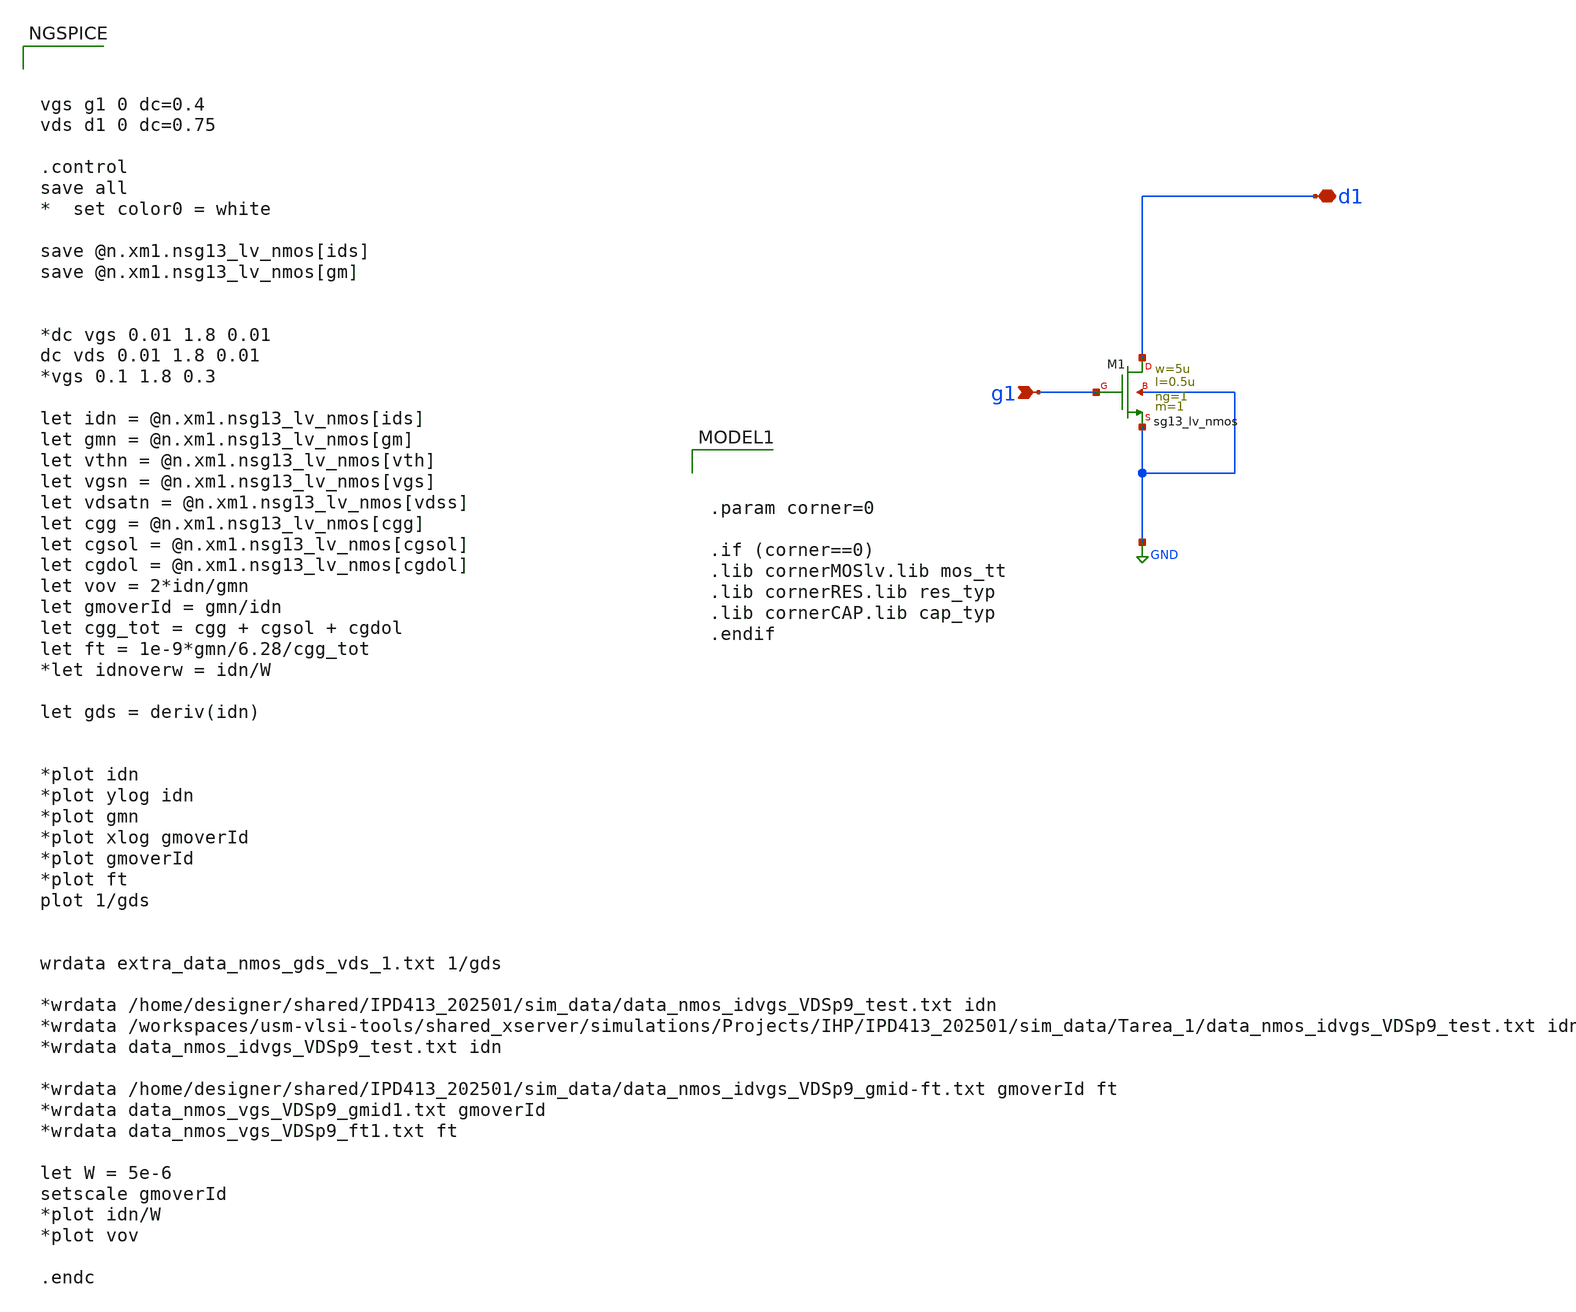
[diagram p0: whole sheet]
** sch_path: others/single mos/tb_nmoslv_charac.sch
**.subckt tb_nmoslv_charac g1 d1
*.ipin g1
*.iopin d1
XM1 d1 g1 GND GND sg13_lv_nmos w=5u l=0.5u ng=1 m=1 mm_ok=1
**** begin user architecture code



vgs g1 0 dc=0.4
vds d1 0 dc=0.75

.control
save all
*  set color0 = white

save @n.xm1.nsg13_lv_nmos[ids]
save @n.xm1.nsg13_lv_nmos[gm]


*dc vgs 0.01 1.8 0.01
dc vds 0.01 1.8 0.01
*vgs 0.1 1.8 0.3

let idn = @n.xm1.nsg13_lv_nmos[ids]
let gmn = @n.xm1.nsg13_lv_nmos[gm]
let vthn = @n.xm1.nsg13_lv_nmos[vth]
let vgsn = @n.xm1.nsg13_lv_nmos[vgs]
let vdsatn = @n.xm1.nsg13_lv_nmos[vdss]
let cgg = @n.xm1.nsg13_lv_nmos[cgg]
let cgsol = @n.xm1.nsg13_lv_nmos[cgsol]
let cgdol = @n.xm1.nsg13_lv_nmos[cgdol]
let vov = 2*idn/gmn
let gmoverId = gmn/idn
let cgg_tot = cgg + cgsol + cgdol
let ft = 1e-9*gmn/6.28/cgg_tot
*let idnoverw = idn/W

let gds = deriv(idn)


*plot idn
*plot ylog idn
*plot gmn
*plot xlog gmoverId
*plot gmoverId
*plot ft
plot 1/gds


wrdata extra_data_nmos_gds_vds_1.txt 1/gds

*wrdata /home/designer/shared/IPD413_202501/sim_data/data_nmos_idvgs_VDSp9_test.txt idn
*wrdata
*+ /workspaces/usm-vlsi-tools/shared_xserver/simulations/Projects/IHP/IPD413_202501/sim_data/Tarea_1/data_nmos_idvgs_VDSp9_test.txt idn
*wrdata data_nmos_idvgs_VDSp9_test.txt idn

*wrdata /home/designer/shared/IPD413_202501/sim_data/data_nmos_idvgs_VDSp9_gmid-ft.txt gmoverId ft
*wrdata data_nmos_vgs_VDSp9_gmid1.txt gmoverId
*wrdata data_nmos_vgs_VDSp9_ft1.txt ft

let W = 5e-6
setscale gmoverId
*plot idn/W
*plot vov

.endc




.param corner=0

.if (corner==0)
.lib cornerMOSlv.lib mos_tt
.lib cornerRES.lib res_typ
.lib cornerCAP.lib cap_typ
.endif

**** end user architecture code
**.ends
.GLOBAL GND
.end
